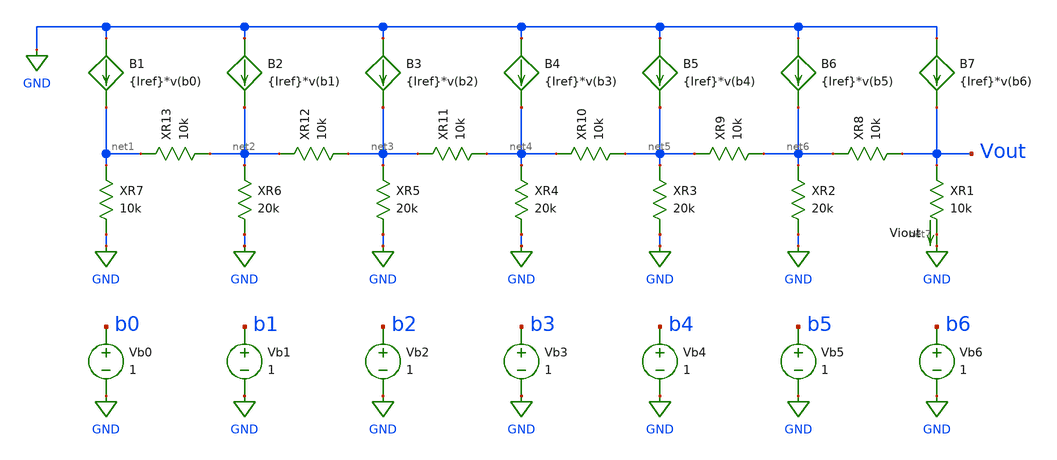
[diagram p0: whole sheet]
** sch_path: mctest/mcdactut.sch
**.subckt mcdactut
B1 GND net1 I={Iref}*v(b0)
Vb0 b0 GND 1
Viout net7 GND 0
.save i(viout)
B2 GND net2 I={Iref}*v(b1)
Vb1 b1 GND 1
B3 GND net3 I={Iref}*v(b2)
Vb2 b2 GND 1
B4 GND net4 I={Iref}*v(b3)
Vb3 b3 GND 1
B5 GND net5 I={Iref}*v(b4)
Vb4 b4 GND 1
B6 GND net6 I={Iref}*v(b5)
Vb5 b5 GND 1
B7 GND Vout I={Iref}*v(b6)
Vb6 b6 GND 1
XR1 Vout net7 gaussres nom=10k
XR2 net6 GND gaussres nom=20k
XR3 net5 GND gaussres nom=20k
XR4 net4 GND gaussres nom=20k
XR5 net3 GND gaussres nom=20k
XR6 net2 GND gaussres nom=20k
XR7 net1 GND gaussres nom=10k
XR8 net6 Vout gaussres nom=10k
XR9 net5 net6 gaussres nom=10k
XR10 net4 net5 gaussres nom=10k
XR11 net3 net4 gaussres nom=10k
XR12 net2 net3 gaussres nom=10k
XR13 net1 net2 gaussres nom=10k
**** begin user architecture code

.param Iref=100u
.control
  set wr_singlescale
  let runs = 10
  let run = 1
  while run <= runs
    set appendwrite = FALSE
    set wr_vecnames
    let code = 0
    while code < 128
      if code eq 0
        let b0 = 0
      else
        let b0 = code % 2
      end
      if floor(code / 2) eq 0
        let b1 = 0
      else
        let b1 = floor(code / 2) % 2
      end
      if floor(code / 4) eq 0
        let b2 = 0
      else
        let b2 = floor(code / 4) % 2
      end
      if floor(code / 8) eq 0
        let b3 = 0
      else
        let b3 = floor(code / 8) % 2
      end
      if floor(code / 16) eq 0
        let b4 = 0
      else
        let b4 = floor(code / 16) % 2
      end
      if floor(code / 32) eq 0
        let b5 = 0
      else
        let b5 = floor(code / 32) % 2
      end
      if floor(code / 64) eq 0
        let b6 = 0
      else
        let b6 = floor(code / 64) % 2
      end
      alter vb0 $&b0
      alter vb1 $&b1
      alter vb2 $&b2
      alter vb3 $&b3
      alter vb4 $&b4
      alter vb5 $&b5
      alter vb6 $&b6
      save all
      op
      wrdata ~/Documents/dactut/mcdactut{$&run}.txt v(b0) v(b1) v(b2) v(b3) v(b4) v(b5) v(b6) i(Viout)
+ v(Vout)
      if code eq 0
        set appendwrite
        set wr_vecnames = FALSE
      end
      let code = code + 1
    end
    reset
    let run = run + 1
  end
  quit
.endc


.param MC_SWITCH=1.0
.subckt gaussres pos neg
.param nom=1k cv=0.005
R1 pos neg {nom + MC_SWITCH*AGAUSS(0,1,1)*cv*nom}
.ends

**** end user architecture code
**.ends
.GLOBAL GND
.end
